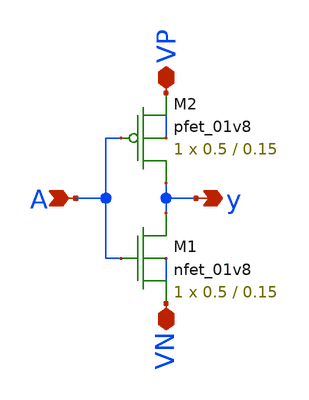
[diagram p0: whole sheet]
** sch_path: and/schematic/inverter.sch
**.subckt inverter VP VN A y
*.iopin VP
*.iopin VN
*.ipin A
*.opin y
XM1 y A VN VN sky130_fd_pr__nfet_01v8 L=0.15 W=0.5 nf=1 ad='int((nf+1)/2) * W/nf * 0.29' as='int((nf+2)/2) * W/nf * 0.29'
+ pd='2*int((nf+1)/2) * (W/nf + 0.29)' ps='2*int((nf+2)/2) * (W/nf + 0.29)' nrd='0.29 / W' nrs='0.29 / W'
+ sa=0 sb=0 sd=0 mult=1 m=1
XM2 y A VP VP sky130_fd_pr__pfet_01v8 L=0.15 W=0.5 nf=1 ad='int((nf+1)/2) * W/nf * 0.29' as='int((nf+2)/2) * W/nf * 0.29'
+ pd='2*int((nf+1)/2) * (W/nf + 0.29)' ps='2*int((nf+2)/2) * (W/nf + 0.29)' nrd='0.29 / W' nrs='0.29 / W'
+ sa=0 sb=0 sd=0 mult=1 m=1
**.ends
.end
